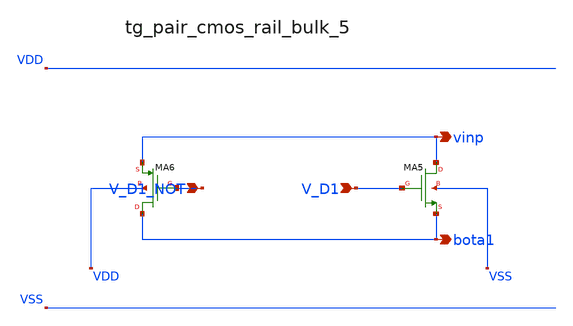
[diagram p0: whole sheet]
** sch_path: analog-db/raw/ia_005_hsu_pga_ideal/hier/blocks/tg_pair_cmos_rail_bulk_5.sch
**.subckt tg_pair_cmos_rail_bulk_5 V_D1_NOT V_D1 vinp bota1
*.ipin V_D1_NOT
*.ipin V_D1
*.opin vinp
*.opin bota1
XMA5 vinp V_D1 bota1 VSS sg13_lv_nmos w=x_dut_xma5_w l=x_dut_xma5_l ng=1 m=x_dut_xma5_m
XMA6 bota1 V_D1_NOT vinp VDD sg13_lv_pmos w=x_dut_xma6_w l=x_dut_xma6_l ng=1 m=x_dut_xma6_m
**.ends
.end
